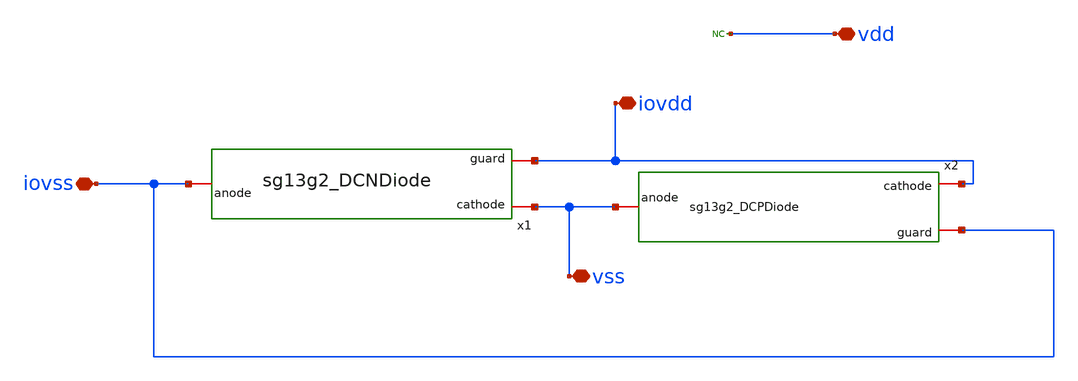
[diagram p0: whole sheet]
** sch_path: design/blocks-std/sg13g2_IOPadVSS/schematic/sg13g2_IOPadVSS.sch
**.subckt sg13g2_IOPadVSS iovss iovdd vss vdd
*.iopin iovss
*.iopin iovdd
*.iopin vss
*.iopin vdd
x1 vss iovss iovdd sg13g2_DCNDiode
x2 iovdd vss iovss sg13g2_DCPDiode
* noconn vdd
**.ends

* expanding   symbol:  blocks-std/sg13g2_DCNDiode/schematic/sg13g2_DCNDiode.sym # of pins=3
** sym_path: blocks-std/sg13g2_DCNDiode/schematic/sg13g2_DCNDiode.sym
** sch_path: blocks-std/sg13g2_DCNDiode/schematic/sg13g2_DCNDiode.sch
.subckt sg13g2_DCNDiode cathode anode guard
*.iopin cathode
*.iopin anode
*.iopin guard
XD1 anode cathode dantenna l=1.26u w=27.78u
XD2 anode cathode dantenna l=1.26u w=27.78u
.ends


* expanding   symbol:  blocks-std/sg13g2_DCPDiode/schematic/sg13g2_DCPDiode.sym # of pins=3
** sym_path: blocks-std/sg13g2_DCPDiode/schematic/sg13g2_DCPDiode.sym
** sch_path: blocks-std/sg13g2_DCPDiode/schematic/sg13g2_DCPDiode.sch
.subckt sg13g2_DCPDiode cathode anode guard
*.iopin cathode
*.iopin anode
*.iopin guard
XD1 anode cathode dpantenna l=1.26u w=27.78u
XD2 anode cathode dpantenna l=1.26u w=27.78u
.ends

.end
